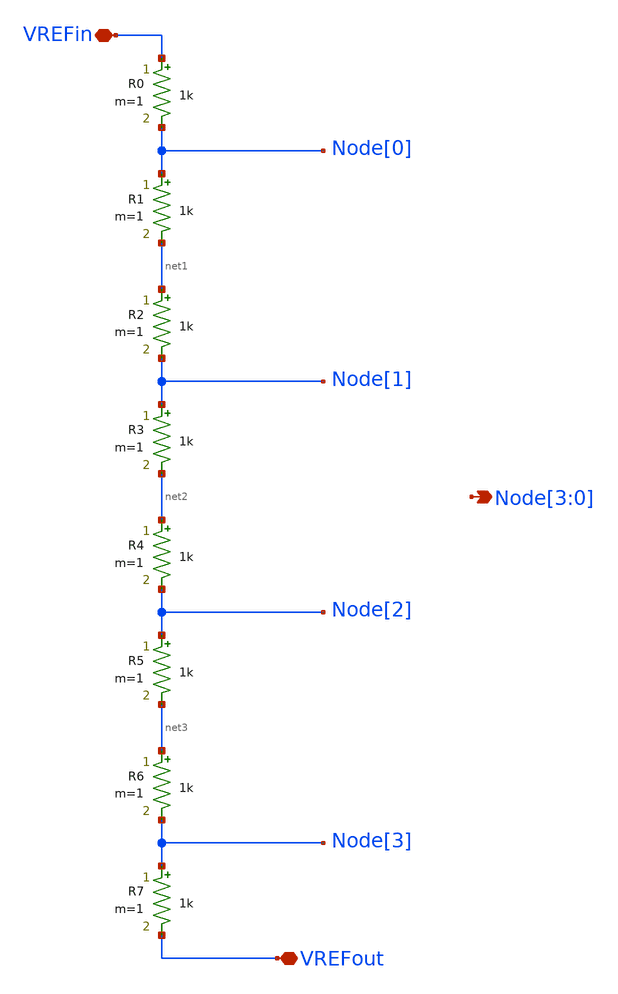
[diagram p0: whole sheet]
** sch_path: ihp130_cells/Resistor_String/ihp130_resistor_string.sch
**.subckt ihp130_resistor_string VREFout VREFin Node[3],Node[2],Node[1],Node[0]
*.iopin VREFout
*.iopin VREFin
*.opin Node[3],Node[2],Node[1],Node[0]
R0 VREFin Node[0] 1k m=1
R1 Node[0] net1 1k m=1
R2 net1 Node[1] 1k m=1
R3 Node[1] net2 1k m=1
R4 net2 Node[2] 1k m=1
R5 Node[2] net3 1k m=1
R6 net3 Node[3] 1k m=1
R7 Node[3] VREFout 1k m=1
**.ends
.end
